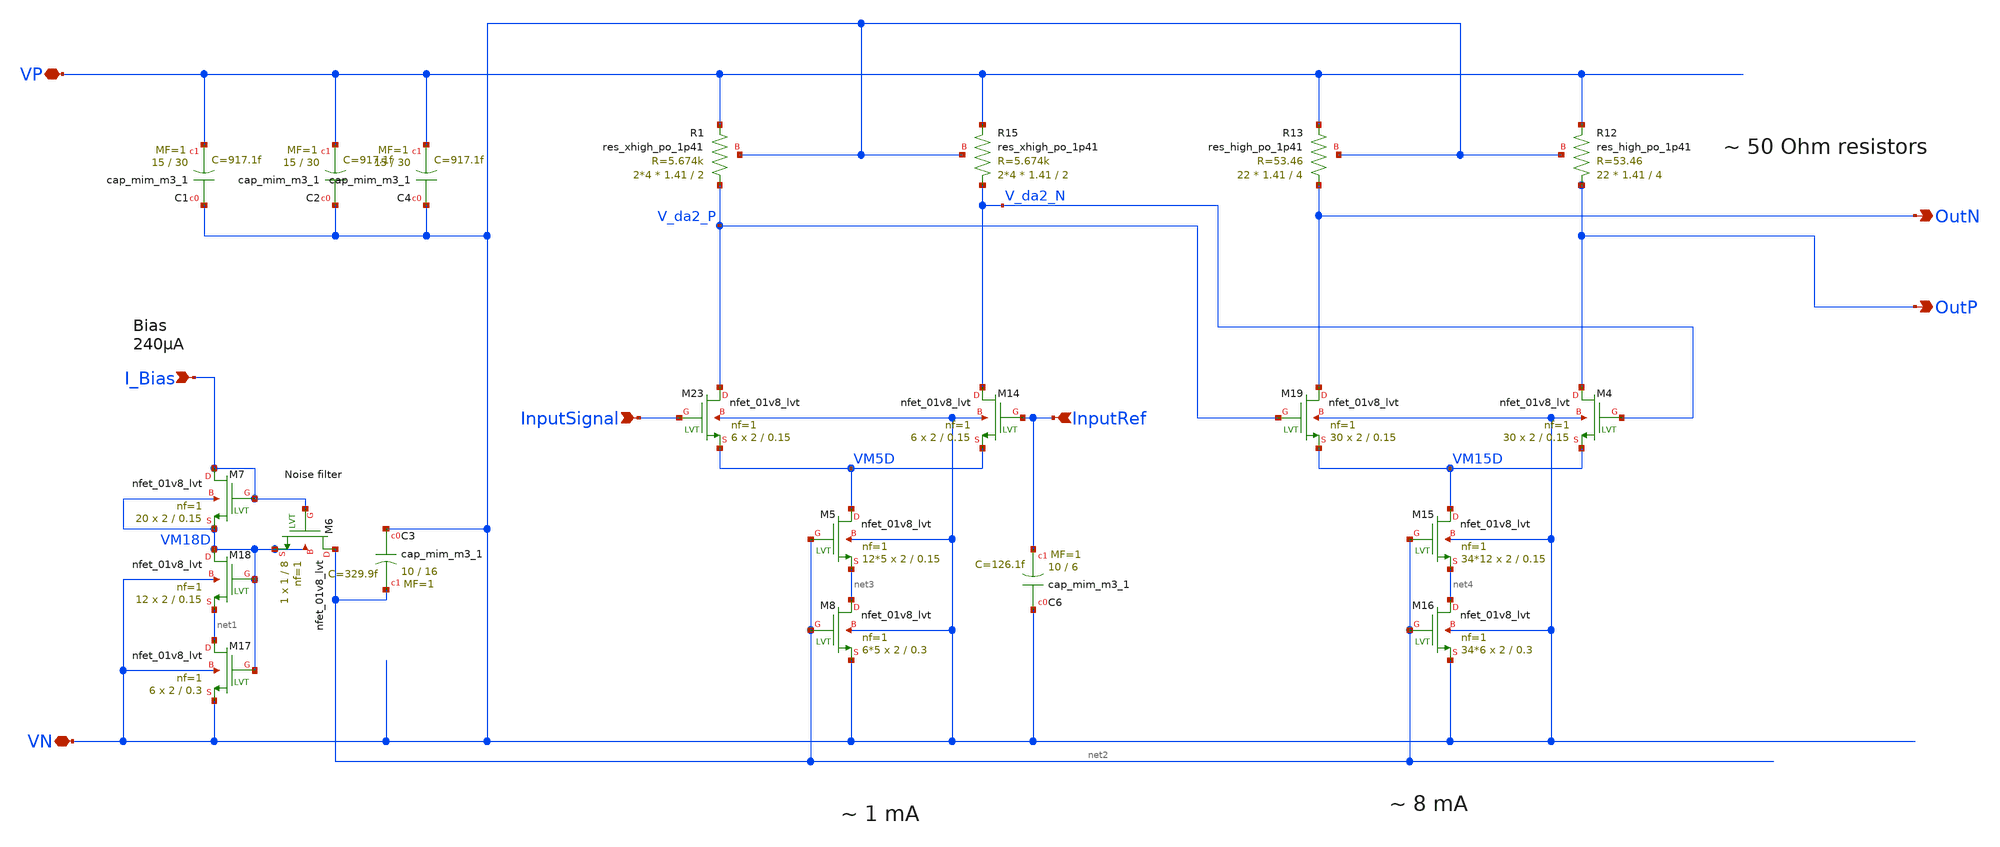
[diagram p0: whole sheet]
** sch_path: xschem/outdriver/outdriver_50ohm_lg.sch
**.subckt outdriver_50ohm_lg VN InputRef VP I_Bias InputSignal OutN OutP
*.iopin VN
*.ipin InputRef
*.iopin VP
*.ipin I_Bias
*.ipin InputSignal
*.opin OutN
*.opin OutP
XM17 net1 VM18D VN VN sky130_fd_pr__nfet_01v8_lvt L=0.3 W=2 nf=1 ad='int((nf+1)/2) * W/nf * 0.29' as='int((nf+2)/2) * W/nf * 0.29'
+ pd='2*int((nf+1)/2) * (W/nf + 0.29)' ps='2*int((nf+2)/2) * (W/nf + 0.29)' nrd='0.29 / W' nrs='0.29 / W'
+ sa=0 sb=0 sd=0 mult=6 m=6
XM18 VM18D VM18D net1 VN sky130_fd_pr__nfet_01v8_lvt L=0.15 W=2 nf=1 ad='int((nf+1)/2) * W/nf * 0.29'
+ as='int((nf+2)/2) * W/nf * 0.29' pd='2*int((nf+1)/2) * (W/nf + 0.29)' ps='2*int((nf+2)/2) * (W/nf + 0.29)'
+ nrd='0.29 / W' nrs='0.29 / W' sa=0 sb=0 sd=0 mult=12 m=12
XM7 I_Bias I_Bias VM18D VM18D sky130_fd_pr__nfet_01v8_lvt L=0.15 W=2 nf=1 ad='int((nf+1)/2) * W/nf * 0.29'
+ as='int((nf+2)/2) * W/nf * 0.29' pd='2*int((nf+1)/2) * (W/nf + 0.29)' ps='2*int((nf+2)/2) * (W/nf + 0.29)'
+ nrd='0.29 / W' nrs='0.29 / W' sa=0 sb=0 sd=0 mult=20 m=20
XM5 VM5D net2 net3 VN sky130_fd_pr__nfet_01v8_lvt L=0.15 W=2 nf=1 ad='int((nf+1)/2) * W/nf * 0.29' as='int((nf+2)/2) * W/nf * 0.29'
+ pd='2*int((nf+1)/2) * (W/nf + 0.29)' ps='2*int((nf+2)/2) * (W/nf + 0.29)' nrd='0.29 / W' nrs='0.29 / W'
+ sa=0 sb=0 sd=0 mult=12*5 m=12*5
XM8 net3 net2 VN VN sky130_fd_pr__nfet_01v8_lvt L=0.3 W=2 nf=1 ad='int((nf+1)/2) * W/nf * 0.29' as='int((nf+2)/2) * W/nf * 0.29'
+ pd='2*int((nf+1)/2) * (W/nf + 0.29)' ps='2*int((nf+2)/2) * (W/nf + 0.29)' nrd='0.29 / W' nrs='0.29 / W'
+ sa=0 sb=0 sd=0 mult=6*5 m=6*5
XM6 net2 I_Bias VM18D VM18D sky130_fd_pr__nfet_01v8_lvt L=8 W=1 nf=1 ad='int((nf+1)/2) * W/nf * 0.29'
+ as='int((nf+2)/2) * W/nf * 0.29' pd='2*int((nf+1)/2) * (W/nf + 0.29)' ps='2*int((nf+2)/2) * (W/nf + 0.29)'
+ nrd='0.29 / W' nrs='0.29 / W' sa=0 sb=0 sd=0 mult=1 m=1
XC1 VN VP sky130_fd_pr__cap_mim_m3_1 W=15 L=30 MF=1 m=1
XM15 VM15D net2 net4 VN sky130_fd_pr__nfet_01v8_lvt L=0.15 W=2 nf=1 ad='int((nf+1)/2) * W/nf * 0.29'
+ as='int((nf+2)/2) * W/nf * 0.29' pd='2*int((nf+1)/2) * (W/nf + 0.29)' ps='2*int((nf+2)/2) * (W/nf + 0.29)'
+ nrd='0.29 / W' nrs='0.29 / W' sa=0 sb=0 sd=0 mult=34*12 m=34*12
XM16 net4 net2 VN VN sky130_fd_pr__nfet_01v8_lvt L=0.3 W=2 nf=1 ad='int((nf+1)/2) * W/nf * 0.29' as='int((nf+2)/2) * W/nf * 0.29'
+ pd='2*int((nf+1)/2) * (W/nf + 0.29)' ps='2*int((nf+2)/2) * (W/nf + 0.29)' nrd='0.29 / W' nrs='0.29 / W'
+ sa=0 sb=0 sd=0 mult=34*6 m=34*6
XM4 OutP V_da2_N VM15D VN sky130_fd_pr__nfet_01v8_lvt L=0.15 W=2 nf=1 ad='int((nf+1)/2) * W/nf * 0.29'
+ as='int((nf+2)/2) * W/nf * 0.29' pd='2*int((nf+1)/2) * (W/nf + 0.29)' ps='2*int((nf+2)/2) * (W/nf + 0.29)'
+ nrd='0.29 / W' nrs='0.29 / W' sa=0 sb=0 sd=0 mult=30 m=30
XM23 V_da2_P InputSignal VM5D VN sky130_fd_pr__nfet_01v8_lvt L=0.15 W=2 nf=1 ad='int((nf+1)/2) * W/nf * 0.29'
+ as='int((nf+2)/2) * W/nf * 0.29' pd='2*int((nf+1)/2) * (W/nf + 0.29)' ps='2*int((nf+2)/2) * (W/nf + 0.29)'
+ nrd='0.29 / W' nrs='0.29 / W' sa=0 sb=0 sd=0 mult=6 m=6
XM19 OutN V_da2_P VM15D VN sky130_fd_pr__nfet_01v8_lvt L=0.15 W=2 nf=1 ad='int((nf+1)/2) * W/nf * 0.29'
+ as='int((nf+2)/2) * W/nf * 0.29' pd='2*int((nf+1)/2) * (W/nf + 0.29)' ps='2*int((nf+2)/2) * (W/nf + 0.29)'
+ nrd='0.29 / W' nrs='0.29 / W' sa=0 sb=0 sd=0 mult=30 m=30
XM14 V_da2_N InputRef VM5D VN sky130_fd_pr__nfet_01v8_lvt L=0.15 W=2 nf=1 ad='int((nf+1)/2) * W/nf * 0.29'
+ as='int((nf+2)/2) * W/nf * 0.29' pd='2*int((nf+1)/2) * (W/nf + 0.29)' ps='2*int((nf+2)/2) * (W/nf + 0.29)'
+ nrd='0.29 / W' nrs='0.29 / W' sa=0 sb=0 sd=0 mult=6 m=6
XR12 OutP VP VN sky130_fd_pr__res_high_po_1p41 L=4 mult=22 m=22
XR13 OutN VP VN sky130_fd_pr__res_high_po_1p41 L=4 mult=22 m=22
XR1 V_da2_P VP VN sky130_fd_pr__res_xhigh_po_1p41 L=2 mult=2*4 m=2*4
XR15 V_da2_N VP VN sky130_fd_pr__res_xhigh_po_1p41 L=2 mult=2*4 m=2*4
XC6 VN InputRef sky130_fd_pr__cap_mim_m3_1 W=10 L=6 MF=1 m=1
XC2 VN VP sky130_fd_pr__cap_mim_m3_1 W=15 L=30 MF=1 m=1
XC4 VN VP sky130_fd_pr__cap_mim_m3_1 W=15 L=30 MF=1 m=1
XC3 VN net2 sky130_fd_pr__cap_mim_m3_1 W=10 L=16 MF=1 m=1
**.ends
.end
